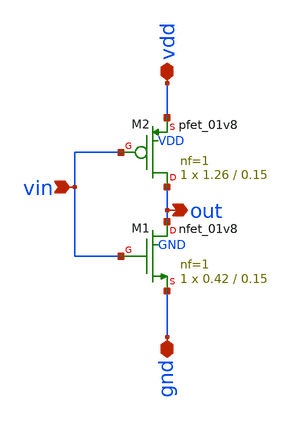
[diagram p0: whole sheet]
** sch_path: xschem/inverter.sch
**.subckt inverter gnd vdd vin out
*.iopin gnd
*.iopin vdd
*.ipin vin
*.opin out
XM1 out vin gnd GND sky130_fd_pr__nfet_01v8 L=0.15 W=0.42 nf=1 ad='int((nf+1)/2) * W/nf * 0.29' as='int((nf+2)/2) * W/nf * 0.29'
+ pd='2*int((nf+1)/2) * (W/nf + 0.29)' ps='2*int((nf+2)/2) * (W/nf + 0.29)' nrd='0.29 / W' nrs='0.29 / W'
+ sa=0 sb=0 sd=0 mult=1 m=1
XM2 out vin vdd VDD sky130_fd_pr__pfet_01v8 L=0.15 W=1.26 nf=1 ad='int((nf+1)/2) * W/nf * 0.29' as='int((nf+2)/2) * W/nf * 0.29'
+ pd='2*int((nf+1)/2) * (W/nf + 0.29)' ps='2*int((nf+2)/2) * (W/nf + 0.29)' nrd='0.29 / W' nrs='0.29 / W'
+ sa=0 sb=0 sd=0 mult=1 m=1
**.ends
.end
